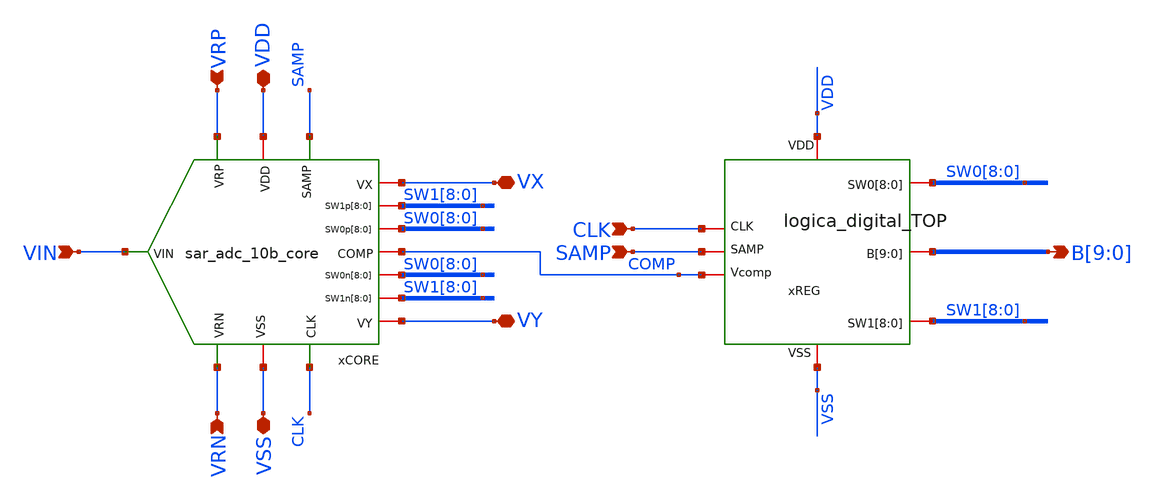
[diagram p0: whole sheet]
** sch_path: designs/sar_adc/top/sar_adc_10b/xschem/sar_adc_10b.sch
**.subckt sar_adc_10b VSS VDD VRP VRN CLK SAMP B[9],B[8],B[7],B[6],B[5],B[4],B[3],B[2],B[1],B[0] VIN
*+ VX VY
*.iopin VSS
*.iopin VDD
*.ipin VRP
*.ipin VRN
*.ipin CLK
*.ipin SAMP
*.opin B[9],B[8],B[7],B[6],B[5],B[4],B[3],B[2],B[1],B[0]
*.ipin VIN
*.iopin VX
*.iopin VY
xREG VDD CLK SAMP COMP SW0[8] SW0[7] SW0[6] SW0[5] SW0[4] SW0[3] SW0[2] SW0[1] SW0[0] B[9] B[8] B[7]
+ B[6] B[5] B[4] B[3] B[2] B[1] B[0] SW1[8] SW1[7] SW1[6] SW1[5] SW1[4] SW1[3] SW1[2] SW1[1] SW1[0] VSS
+ logica_digital_TOP
xCORE SW1[8] SW1[7] SW1[6] SW1[5] SW1[4] SW1[3] SW1[2] SW1[1] SW1[0] SW0[8] SW0[7] SW0[6] SW0[5]
+ SW0[4] SW0[3] SW0[2] SW0[1] SW0[0] SW1[8] SW1[7] SW1[6] SW1[5] SW1[4] SW1[3] SW1[2] SW1[1] SW1[0] SW0[8]
+ SW0[7] SW0[6] SW0[5] SW0[4] SW0[3] SW0[2] SW0[1] SW0[0] VX COMP VY VIN VDD VSS VRP SAMP CLK VRN
+ sar_adc_10b_core
**.ends
.end
